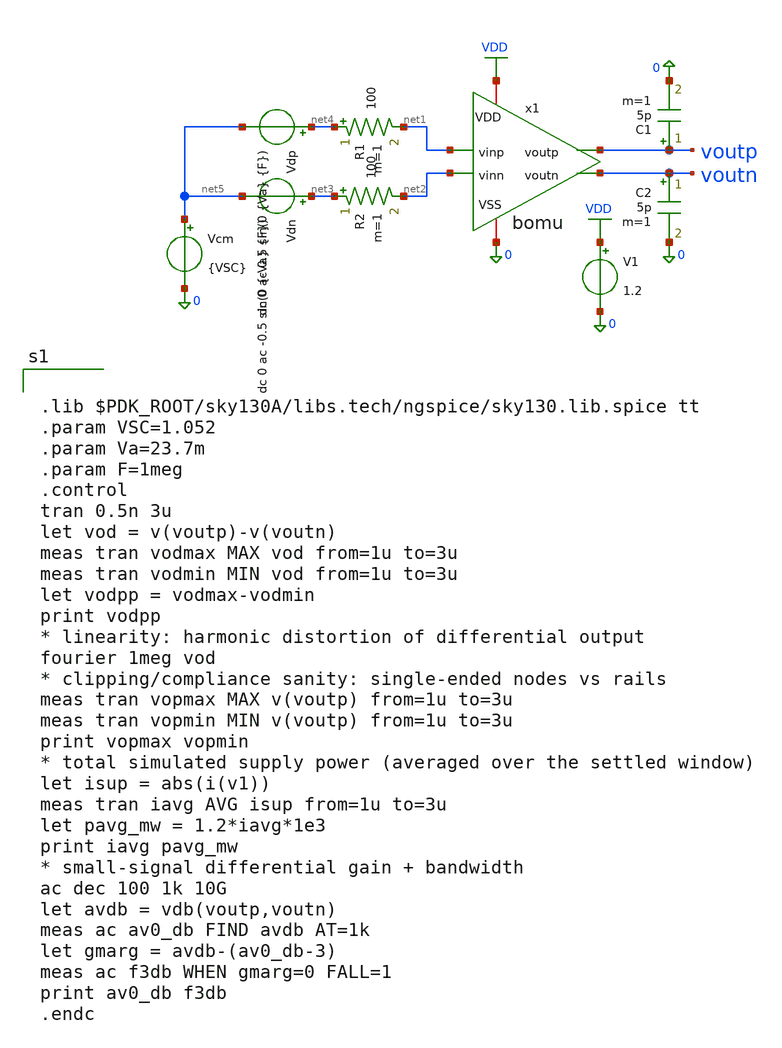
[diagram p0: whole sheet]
** sch_path: ip/tb_bomu_swing.sch
**.subckt tb_bomu_swing
x1 net1 net2 voutp voutn VDD 0 bomu
V1 VDD 0 1.2
R1 net4 net1 100 m=1
R2 net3 net2 100 m=1
Vdp net4 net5 dc 0 ac 0.5 sin(0 {Va} {F})
Vdn net3 net5 dc 0 ac -0.5 sin(0 {-Va} {F})
Vcm net5 0 {VSC}
C1 voutp 0 5p m=1
C2 voutn 0 5p m=1
**** begin user architecture code


.lib $PDK_ROOT/sky130A/libs.tech/ngspice/sky130.lib.spice tt
.param VSC=1.052
.param Va=23.7m
.param F=1meg
.control
tran 0.5n 3u
let vod = v(voutp)-v(voutn)
meas tran vodmax MAX vod from=1u to=3u
meas tran vodmin MIN vod from=1u to=3u
let vodpp = vodmax-vodmin
print vodpp
* linearity: harmonic distortion of differential output
fourier 1meg vod
* clipping/compliance sanity: single-ended nodes vs rails
meas tran vopmax MAX v(voutp) from=1u to=3u
meas tran vopmin MIN v(voutp) from=1u to=3u
print vopmax vopmin
* total simulated supply power (averaged over the settled window)
let isup = abs(i(v1))
meas tran iavg AVG isup from=1u to=3u
let pavg_mw = 1.2*iavg*1e3
print iavg pavg_mw
* small-signal differential gain + bandwidth
ac dec 100 1k 10G
let avdb = vdb(voutp,voutn)
meas ac av0_db FIND avdb AT=1k
let gmarg = avdb-(av0_db-3)
meas ac f3db WHEN gmarg=0 FALL=1
print av0_db f3db
.endc

**** end user architecture code
**.ends

* expanding   symbol:  /foss/designs/BoMu-tt-sky130a/ip/bomu.sym # of pins=6
** sym_path: ip/bomu.sym
** sch_path: ip/bomu.sch
.subckt bomu vinp vinn voutp voutn VDD VSS
*.ipin vinp
*.ipin vinn
*.opin voutn
*.opin voutp
*.iopin VDD
*.iopin VSS
XRD1 voutn VDD VSS sky130_fd_pr__res_high_po_5p73 L=2.21 mult=1 m=1
XRD2 voutp VDD VSS sky130_fd_pr__res_high_po_5p73 L=2.21 mult=1 m=1
XM1 voutn vinp vtail VSS sky130_fd_pr__nfet_01v8_lvt L=0.15 W=320 nf=32 ad=0 as=0 pd=0 ps=0 nrd=0
+ nrs=0 sa=0 sb=0 sd=0 mult=1 m=1
XM2 voutp vinn vtail VSS sky130_fd_pr__nfet_01v8_lvt L=0.15 W=320 nf=32 ad=0 as=0 pd=0 ps=0 nrd=0
+ nrs=0 sa=0 sb=0 sd=0 mult=1 m=1
XRref nbias VDD VSS sky130_fd_pr__res_high_po_2p85 L=1.74 mult=1 m=1
XM3 vtail nbias VSS VSS sky130_fd_pr__nfet_01v8 L=0.5 W=80 nf=8 ad=0 as=0 pd=0 ps=0 nrd=0 nrs=0 sa=0
+ sb=0 sd=0 mult=1 m=1
XM4 nbias nbias VSS VSS sky130_fd_pr__nfet_01v8 L=0.5 W=10 nf=1 ad=0 as=0 pd=0 ps=0 nrd=0 nrs=0 sa=0
+ sb=0 sd=0 mult=1 m=1
XRdum1 VSS VSS VSS sky130_fd_pr__res_high_po_5p73 L=2.21 mult=1 m=1
XRdum2 VSS VSS VSS sky130_fd_pr__res_high_po_5p73 L=2.21 mult=1 m=1
XMdum VSS VSS VSS VSS sky130_fd_pr__nfet_01v8_lvt L=0.15 W=10 nf=1 ad=0 as=0 pd=0 ps=0 nrd=0 nrs=0
+ sa=0 sb=0 sd=0 mult=4 m=4
.ends

.GLOBAL VDD
.end
